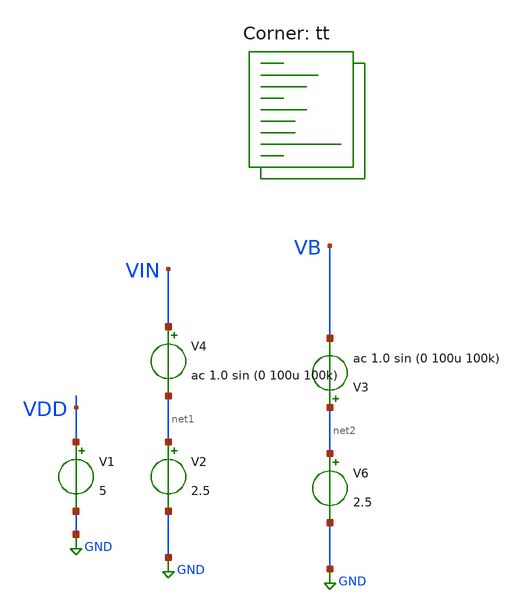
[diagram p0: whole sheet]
** sch_path: old stuff/my_amp_test/differential_stage/cmfb_op_amp.sch
**.subckt cmfb_op_amp
V1 VDD GND 5
V2 net1 GND 2.5
V6 net2 GND 2.5
V4 VIN net1 ac 1.0 sin (0 100u 100k)
V3 net2 VB ac 1.0 sin (0 100u 100k)
**** begin user architecture code

**************************************************************
**************************************************************
**************************************************************
**************************************************************
**************************************************************
*LIBs*********************************************************
**************************************************************
**************************************************************
**************************************************************
**************************************************************
**************************************************************
*.lib $::SKYWATER_MODELS/sky130.lib.spice tt
* chose the corners in the corner file
* tt_mm for mismatch
* ss ff sf fs standart corners
* ll hh lh hl capacitor and resistors corners
* mc for total process variation including corners
**************************************************************
**************************************************************
**************************************************************
**************************************************************
**************************************************************
*Corners/montecarlo options***********************************
**************************************************************
**************************************************************
**************************************************************
**************************************************************
**************************************************************
.TEMP 27
**************************************************************
**************************************************************
**************************************************************
**************************************************************
*SIMULATION and Plots*****************************************
**************************************************************
**************************************************************
**************************************************************
**************************************************************
.control
save all
dc V2 0 5 0.001
plot v(VOUT+) v(VOUT-) deriv(v(VOUT+)) deriv(v(VOUT-))
plot v(VOUT2+) v(VOUT2-) deriv(v(VOUT2+)) deriv(v(VOUT2-))
*plot v(VA)
*plot i(Vmeas)
ac dec 20 1 1000G
plot db(v(VOUT+))
plot db(v(VOUT2+)) phase(v(VOUT+))
.endc

.lib $::SKYWATER_MODELS/sky130.lib.spice tt
**** end user architecture code
**.ends
.GLOBAL GND
.end
